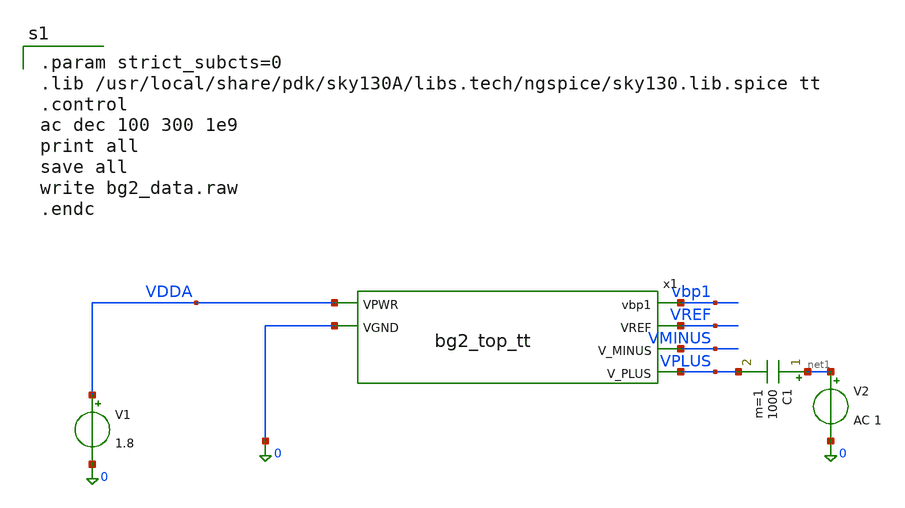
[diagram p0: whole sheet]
** sch_path: lef/lef/gds/bg2_top_tt_ac_tb.sch
**.subckt bg2_top_tt_ac_tb
V1 VDDA 0 1.8
x1 VDDA vbp1 VREF VMINUS VPLUS 0 bg2_top_tt
V2 net1 0 AC 1
C1 net1 VPLUS 1000 m=1
**** begin user architecture code

.param strict_subcts=0
.lib /usr/local/share/pdk/sky130A/libs.tech/ngspice/sky130.lib.spice tt
.control
ac dec 100 300 1e9
print all
save all
write bg2_data.raw
.endc

**** end user architecture code
**.ends
.end
